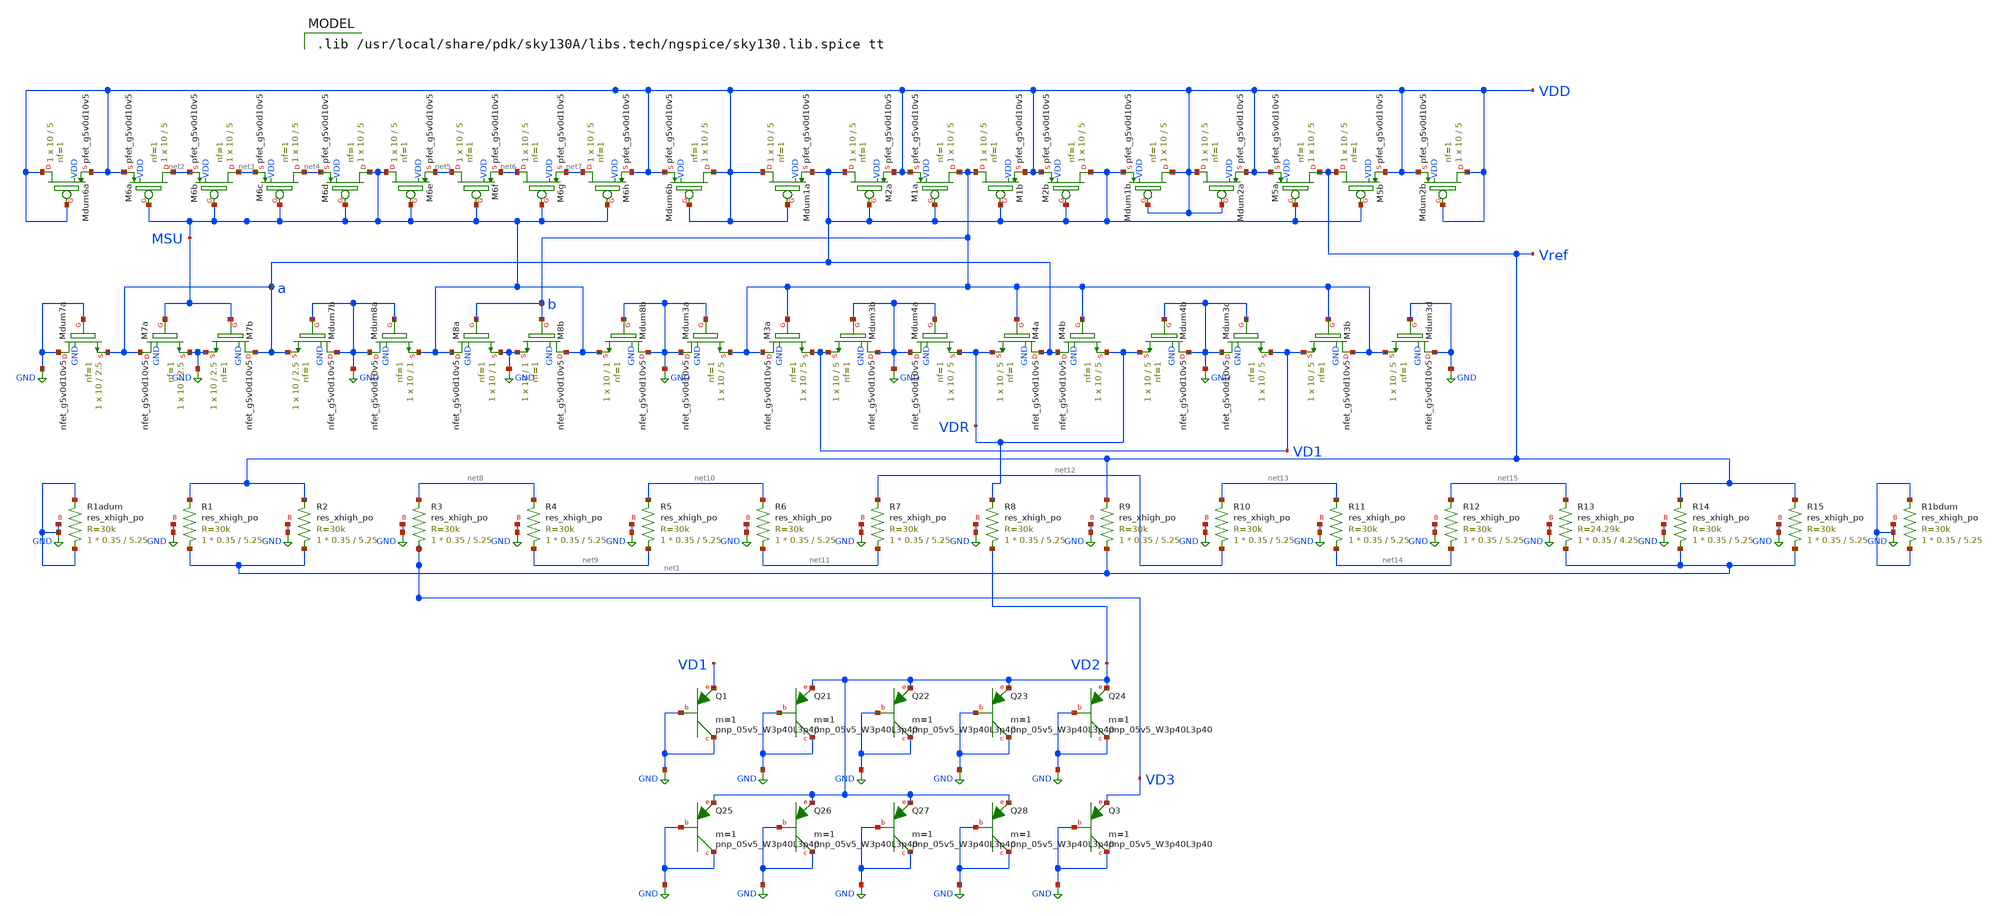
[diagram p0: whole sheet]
** sch_path: 2_BGR_nocas_30k_3p4pnp_floor_Layout.sch
**.subckt 2_BGR_nocas_30k_3p4pnp_floor_Layout
XM2a a a VDD VDD sky130_fd_pr__pfet_g5v0d10v5 L=5 W=10 nf=1 ad='int((nf+1)/2) * W/nf * 0.29' as='int((nf+2)/2) * W/nf * 0.29'
+ pd='2*int((nf+1)/2) * (W/nf + 0.29)' ps='2*int((nf+2)/2) * (W/nf + 0.29)' nrd='0.29 / W' nrs='0.29 / W'
+ sa=0 sb=0 sd=0 mult=1 m=1
XM1a b a VDD VDD sky130_fd_pr__pfet_g5v0d10v5 L=5 W=10 nf=1 ad='int((nf+1)/2) * W/nf * 0.29' as='int((nf+2)/2) * W/nf * 0.29'
+ pd='2*int((nf+1)/2) * (W/nf + 0.29)' ps='2*int((nf+2)/2) * (W/nf + 0.29)' nrd='0.29 / W' nrs='0.29 / W'
+ sa=0 sb=0 sd=0 mult=1 m=1
XM1b b a VDD VDD sky130_fd_pr__pfet_g5v0d10v5 L=5 W=10 nf=1 ad='int((nf+1)/2) * W/nf * 0.29' as='int((nf+2)/2) * W/nf * 0.29'
+ pd='2*int((nf+1)/2) * (W/nf + 0.29)' ps='2*int((nf+2)/2) * (W/nf + 0.29)' nrd='0.29 / W' nrs='0.29 / W'
+ sa=0 sb=0 sd=0 mult=1 m=1
XM2b a a VDD VDD sky130_fd_pr__pfet_g5v0d10v5 L=5 W=10 nf=1 ad='int((nf+1)/2) * W/nf * 0.29' as='int((nf+2)/2) * W/nf * 0.29'
+ pd='2*int((nf+1)/2) * (W/nf + 0.29)' ps='2*int((nf+2)/2) * (W/nf + 0.29)' nrd='0.29 / W' nrs='0.29 / W'
+ sa=0 sb=0 sd=0 mult=1 m=1
XM5a Vref a VDD VDD sky130_fd_pr__pfet_g5v0d10v5 L=5 W=10 nf=1 ad='int((nf+1)/2) * W/nf * 0.29' as='int((nf+2)/2) * W/nf * 0.29'
+ pd='2*int((nf+1)/2) * (W/nf + 0.29)' ps='2*int((nf+2)/2) * (W/nf + 0.29)' nrd='0.29 / W' nrs='0.29 / W'
+ sa=0 sb=0 sd=0 mult=1 m=1
XM5b Vref a VDD VDD sky130_fd_pr__pfet_g5v0d10v5 L=5 W=10 nf=1 ad='int((nf+1)/2) * W/nf * 0.29' as='int((nf+2)/2) * W/nf * 0.29'
+ pd='2*int((nf+1)/2) * (W/nf + 0.29)' ps='2*int((nf+2)/2) * (W/nf + 0.29)' nrd='0.29 / W' nrs='0.29 / W'
+ sa=0 sb=0 sd=0 mult=1 m=1
XQ21 GND GND VD2 sky130_fd_pr__pnp_05v5_W3p40L3p40 m=1
XQ22 GND GND VD2 sky130_fd_pr__pnp_05v5_W3p40L3p40 m=1
XQ23 GND GND VD2 sky130_fd_pr__pnp_05v5_W3p40L3p40 m=1
XQ24 GND GND VD2 sky130_fd_pr__pnp_05v5_W3p40L3p40 m=1
XQ1 GND GND VD1 sky130_fd_pr__pnp_05v5_W3p40L3p40 m=1
XQ26 GND GND VD2 sky130_fd_pr__pnp_05v5_W3p40L3p40 m=1
XQ27 GND GND VD2 sky130_fd_pr__pnp_05v5_W3p40L3p40 m=1
XQ28 GND GND VD2 sky130_fd_pr__pnp_05v5_W3p40L3p40 m=1
XQ3 GND GND VD3 sky130_fd_pr__pnp_05v5_W3p40L3p40 m=1
XQ25 GND GND VD2 sky130_fd_pr__pnp_05v5_W3p40L3p40 m=1
XMdum1a VDD VDD a VDD sky130_fd_pr__pfet_g5v0d10v5 L=5 W=10 nf=1 ad='int((nf+1)/2) * W/nf * 0.29' as='int((nf+2)/2) * W/nf * 0.29'
+ pd='2*int((nf+1)/2) * (W/nf + 0.29)' ps='2*int((nf+2)/2) * (W/nf + 0.29)' nrd='0.29 / W' nrs='0.29 / W'
+ sa=0 sb=0 sd=0 mult=1 m=1
XMdum1b VDD VDD a VDD sky130_fd_pr__pfet_g5v0d10v5 L=5 W=10 nf=1 ad='int((nf+1)/2) * W/nf * 0.29' as='int((nf+2)/2) * W/nf * 0.29'
+ pd='2*int((nf+1)/2) * (W/nf + 0.29)' ps='2*int((nf+2)/2) * (W/nf + 0.29)' nrd='0.29 / W' nrs='0.29 / W'
+ sa=0 sb=0 sd=0 mult=1 m=1
XMdum2a VDD VDD VDD VDD sky130_fd_pr__pfet_g5v0d10v5 L=5 W=10 nf=1 ad='int((nf+1)/2) * W/nf * 0.29' as='int((nf+2)/2) * W/nf * 0.29'
+ pd='2*int((nf+1)/2) * (W/nf + 0.29)' ps='2*int((nf+2)/2) * (W/nf + 0.29)' nrd='0.29 / W' nrs='0.29 / W'
+ sa=0 sb=0 sd=0 mult=1 m=1
XMdum2b VDD VDD VDD VDD sky130_fd_pr__pfet_g5v0d10v5 L=5 W=10 nf=1 ad='int((nf+1)/2) * W/nf * 0.29' as='int((nf+2)/2) * W/nf * 0.29'
+ pd='2*int((nf+1)/2) * (W/nf + 0.29)' ps='2*int((nf+2)/2) * (W/nf + 0.29)' nrd='0.29 / W' nrs='0.29 / W'
+ sa=0 sb=0 sd=0 mult=1 m=1
XM6a net2 MSU VDD VDD sky130_fd_pr__pfet_g5v0d10v5 L=5 W=10 nf=1 ad='int((nf+1)/2) * W/nf * 0.29' as='int((nf+2)/2) * W/nf * 0.29'
+ pd='2*int((nf+1)/2) * (W/nf + 0.29)' ps='2*int((nf+2)/2) * (W/nf + 0.29)' nrd='0.29 / W' nrs='0.29 / W'
+ sa=0 sb=0 sd=0 mult=1 m=1
XM6b net3 MSU net2 VDD sky130_fd_pr__pfet_g5v0d10v5 L=5 W=10 nf=1 ad='int((nf+1)/2) * W/nf * 0.29' as='int((nf+2)/2) * W/nf * 0.29'
+ pd='2*int((nf+1)/2) * (W/nf + 0.29)' ps='2*int((nf+2)/2) * (W/nf + 0.29)' nrd='0.29 / W' nrs='0.29 / W'
+ sa=0 sb=0 sd=0 mult=1 m=1
XM6c net4 MSU net3 VDD sky130_fd_pr__pfet_g5v0d10v5 L=5 W=10 nf=1 ad='int((nf+1)/2) * W/nf * 0.29' as='int((nf+2)/2) * W/nf * 0.29'
+ pd='2*int((nf+1)/2) * (W/nf + 0.29)' ps='2*int((nf+2)/2) * (W/nf + 0.29)' nrd='0.29 / W' nrs='0.29 / W'
+ sa=0 sb=0 sd=0 mult=1 m=1
XM6d MSU MSU net4 VDD sky130_fd_pr__pfet_g5v0d10v5 L=5 W=10 nf=1 ad='int((nf+1)/2) * W/nf * 0.29' as='int((nf+2)/2) * W/nf * 0.29'
+ pd='2*int((nf+1)/2) * (W/nf + 0.29)' ps='2*int((nf+2)/2) * (W/nf + 0.29)' nrd='0.29 / W' nrs='0.29 / W'
+ sa=0 sb=0 sd=0 mult=1 m=1
XM6e MSU MSU net5 VDD sky130_fd_pr__pfet_g5v0d10v5 L=5 W=10 nf=1 ad='int((nf+1)/2) * W/nf * 0.29' as='int((nf+2)/2) * W/nf * 0.29'
+ pd='2*int((nf+1)/2) * (W/nf + 0.29)' ps='2*int((nf+2)/2) * (W/nf + 0.29)' nrd='0.29 / W' nrs='0.29 / W'
+ sa=0 sb=0 sd=0 mult=1 m=1
XM6f net5 MSU net6 VDD sky130_fd_pr__pfet_g5v0d10v5 L=5 W=10 nf=1 ad='int((nf+1)/2) * W/nf * 0.29' as='int((nf+2)/2) * W/nf * 0.29'
+ pd='2*int((nf+1)/2) * (W/nf + 0.29)' ps='2*int((nf+2)/2) * (W/nf + 0.29)' nrd='0.29 / W' nrs='0.29 / W'
+ sa=0 sb=0 sd=0 mult=1 m=1
XM6g net6 MSU net7 VDD sky130_fd_pr__pfet_g5v0d10v5 L=5 W=10 nf=1 ad='int((nf+1)/2) * W/nf * 0.29' as='int((nf+2)/2) * W/nf * 0.29'
+ pd='2*int((nf+1)/2) * (W/nf + 0.29)' ps='2*int((nf+2)/2) * (W/nf + 0.29)' nrd='0.29 / W' nrs='0.29 / W'
+ sa=0 sb=0 sd=0 mult=1 m=1
XM6h net7 MSU VDD VDD sky130_fd_pr__pfet_g5v0d10v5 L=5 W=10 nf=1 ad='int((nf+1)/2) * W/nf * 0.29' as='int((nf+2)/2) * W/nf * 0.29'
+ pd='2*int((nf+1)/2) * (W/nf + 0.29)' ps='2*int((nf+2)/2) * (W/nf + 0.29)' nrd='0.29 / W' nrs='0.29 / W'
+ sa=0 sb=0 sd=0 mult=1 m=1
XMdum6b VDD VDD VDD VDD sky130_fd_pr__pfet_g5v0d10v5 L=5 W=10 nf=1 ad='int((nf+1)/2) * W/nf * 0.29' as='int((nf+2)/2) * W/nf * 0.29'
+ pd='2*int((nf+1)/2) * (W/nf + 0.29)' ps='2*int((nf+2)/2) * (W/nf + 0.29)' nrd='0.29 / W' nrs='0.29 / W'
+ sa=0 sb=0 sd=0 mult=1 m=1
XMdum6a VDD VDD VDD VDD sky130_fd_pr__pfet_g5v0d10v5 L=5 W=10 nf=1 ad='int((nf+1)/2) * W/nf * 0.29' as='int((nf+2)/2) * W/nf * 0.29'
+ pd='2*int((nf+1)/2) * (W/nf + 0.29)' ps='2*int((nf+2)/2) * (W/nf + 0.29)' nrd='0.29 / W' nrs='0.29 / W'
+ sa=0 sb=0 sd=0 mult=1 m=1
XM7a a MSU GND GND sky130_fd_pr__nfet_g5v0d10v5 L=2.5 W=10 nf=1 ad='int((nf+1)/2) * W/nf * 0.29' as='int((nf+2)/2) * W/nf * 0.29'
+ pd='2*int((nf+1)/2) * (W/nf + 0.29)' ps='2*int((nf+2)/2) * (W/nf + 0.29)' nrd='0.29 / W' nrs='0.29 / W'
+ sa=0 sb=0 sd=0 mult=1 m=1
XM7b a MSU GND GND sky130_fd_pr__nfet_g5v0d10v5 L=2.5 W=10 nf=1 ad='int((nf+1)/2) * W/nf * 0.29' as='int((nf+2)/2) * W/nf * 0.29'
+ pd='2*int((nf+1)/2) * (W/nf + 0.29)' ps='2*int((nf+2)/2) * (W/nf + 0.29)' nrd='0.29 / W' nrs='0.29 / W'
+ sa=0 sb=0 sd=0 mult=1 m=1
XMdum7a GND GND a GND sky130_fd_pr__nfet_g5v0d10v5 L=2.5 W=10 nf=1 ad='int((nf+1)/2) * W/nf * 0.29' as='int((nf+2)/2) * W/nf * 0.29'
+ pd='2*int((nf+1)/2) * (W/nf + 0.29)' ps='2*int((nf+2)/2) * (W/nf + 0.29)' nrd='0.29 / W' nrs='0.29 / W'
+ sa=0 sb=0 sd=0 mult=1 m=1
XMdum7b GND GND a GND sky130_fd_pr__nfet_g5v0d10v5 L=2.5 W=10 nf=1 ad='int((nf+1)/2) * W/nf * 0.29' as='int((nf+2)/2) * W/nf * 0.29'
+ pd='2*int((nf+1)/2) * (W/nf + 0.29)' ps='2*int((nf+2)/2) * (W/nf + 0.29)' nrd='0.29 / W' nrs='0.29 / W'
+ sa=0 sb=0 sd=0 mult=1 m=1
XMdum8a GND GND MSU GND sky130_fd_pr__nfet_g5v0d10v5 L=1 W=10 nf=1 ad='int((nf+1)/2) * W/nf * 0.29' as='int((nf+2)/2) * W/nf * 0.29'
+ pd='2*int((nf+1)/2) * (W/nf + 0.29)' ps='2*int((nf+2)/2) * (W/nf + 0.29)' nrd='0.29 / W' nrs='0.29 / W'
+ sa=0 sb=0 sd=0 mult=1 m=1
XM8a MSU b GND GND sky130_fd_pr__nfet_g5v0d10v5 L=1 W=10 nf=1 ad='int((nf+1)/2) * W/nf * 0.29' as='int((nf+2)/2) * W/nf * 0.29'
+ pd='2*int((nf+1)/2) * (W/nf + 0.29)' ps='2*int((nf+2)/2) * (W/nf + 0.29)' nrd='0.29 / W' nrs='0.29 / W'
+ sa=0 sb=0 sd=0 mult=1 m=1
XM8b MSU b GND GND sky130_fd_pr__nfet_g5v0d10v5 L=1 W=10 nf=1 ad='int((nf+1)/2) * W/nf * 0.29' as='int((nf+2)/2) * W/nf * 0.29'
+ pd='2*int((nf+1)/2) * (W/nf + 0.29)' ps='2*int((nf+2)/2) * (W/nf + 0.29)' nrd='0.29 / W' nrs='0.29 / W'
+ sa=0 sb=0 sd=0 mult=1 m=1
XMdum8b GND GND MSU GND sky130_fd_pr__nfet_g5v0d10v5 L=1 W=10 nf=1 ad='int((nf+1)/2) * W/nf * 0.29' as='int((nf+2)/2) * W/nf * 0.29'
+ pd='2*int((nf+1)/2) * (W/nf + 0.29)' ps='2*int((nf+2)/2) * (W/nf + 0.29)' nrd='0.29 / W' nrs='0.29 / W'
+ sa=0 sb=0 sd=0 mult=1 m=1
XMdum3a GND GND b GND sky130_fd_pr__nfet_g5v0d10v5 L=5 W=10 nf=1 ad='int((nf+1)/2) * W/nf * 0.29' as='int((nf+2)/2) * W/nf * 0.29'
+ pd='2*int((nf+1)/2) * (W/nf + 0.29)' ps='2*int((nf+2)/2) * (W/nf + 0.29)' nrd='0.29 / W' nrs='0.29 / W'
+ sa=0 sb=0 sd=0 mult=1 m=1
XM3a b b VD1 GND sky130_fd_pr__nfet_g5v0d10v5 L=5 W=10 nf=1 ad='int((nf+1)/2) * W/nf * 0.29' as='int((nf+2)/2) * W/nf * 0.29'
+ pd='2*int((nf+1)/2) * (W/nf + 0.29)' ps='2*int((nf+2)/2) * (W/nf + 0.29)' nrd='0.29 / W' nrs='0.29 / W'
+ sa=0 sb=0 sd=0 mult=1 m=1
XMdum3b GND GND VD1 GND sky130_fd_pr__nfet_g5v0d10v5 L=5 W=10 nf=1 ad='int((nf+1)/2) * W/nf * 0.29' as='int((nf+2)/2) * W/nf * 0.29'
+ pd='2*int((nf+1)/2) * (W/nf + 0.29)' ps='2*int((nf+2)/2) * (W/nf + 0.29)' nrd='0.29 / W' nrs='0.29 / W'
+ sa=0 sb=0 sd=0 mult=1 m=1
XMdum4a GND GND VDR GND sky130_fd_pr__nfet_g5v0d10v5 L=5 W=10 nf=1 ad='int((nf+1)/2) * W/nf * 0.29' as='int((nf+2)/2) * W/nf * 0.29'
+ pd='2*int((nf+1)/2) * (W/nf + 0.29)' ps='2*int((nf+2)/2) * (W/nf + 0.29)' nrd='0.29 / W' nrs='0.29 / W'
+ sa=0 sb=0 sd=0 mult=1 m=1
XM4a a b VDR GND sky130_fd_pr__nfet_g5v0d10v5 L=5 W=10 nf=1 ad='int((nf+1)/2) * W/nf * 0.29' as='int((nf+2)/2) * W/nf * 0.29'
+ pd='2*int((nf+1)/2) * (W/nf + 0.29)' ps='2*int((nf+2)/2) * (W/nf + 0.29)' nrd='0.29 / W' nrs='0.29 / W'
+ sa=0 sb=0 sd=0 mult=1 m=1
XM4b a b VDR GND sky130_fd_pr__nfet_g5v0d10v5 L=5 W=10 nf=1 ad='int((nf+1)/2) * W/nf * 0.29' as='int((nf+2)/2) * W/nf * 0.29'
+ pd='2*int((nf+1)/2) * (W/nf + 0.29)' ps='2*int((nf+2)/2) * (W/nf + 0.29)' nrd='0.29 / W' nrs='0.29 / W'
+ sa=0 sb=0 sd=0 mult=1 m=1
XMdum4b GND GND VDR GND sky130_fd_pr__nfet_g5v0d10v5 L=5 W=10 nf=1 ad='int((nf+1)/2) * W/nf * 0.29' as='int((nf+2)/2) * W/nf * 0.29'
+ pd='2*int((nf+1)/2) * (W/nf + 0.29)' ps='2*int((nf+2)/2) * (W/nf + 0.29)' nrd='0.29 / W' nrs='0.29 / W'
+ sa=0 sb=0 sd=0 mult=1 m=1
XMdum3c GND GND VD1 GND sky130_fd_pr__nfet_g5v0d10v5 L=5 W=10 nf=1 ad='int((nf+1)/2) * W/nf * 0.29' as='int((nf+2)/2) * W/nf * 0.29'
+ pd='2*int((nf+1)/2) * (W/nf + 0.29)' ps='2*int((nf+2)/2) * (W/nf + 0.29)' nrd='0.29 / W' nrs='0.29 / W'
+ sa=0 sb=0 sd=0 mult=1 m=1
XM3b b b VD1 GND sky130_fd_pr__nfet_g5v0d10v5 L=5 W=10 nf=1 ad='int((nf+1)/2) * W/nf * 0.29' as='int((nf+2)/2) * W/nf * 0.29'
+ pd='2*int((nf+1)/2) * (W/nf + 0.29)' ps='2*int((nf+2)/2) * (W/nf + 0.29)' nrd='0.29 / W' nrs='0.29 / W'
+ sa=0 sb=0 sd=0 mult=1 m=1
XMdum3d GND GND b GND sky130_fd_pr__nfet_g5v0d10v5 L=5 W=10 nf=1 ad='int((nf+1)/2) * W/nf * 0.29' as='int((nf+2)/2) * W/nf * 0.29'
+ pd='2*int((nf+1)/2) * (W/nf + 0.29)' ps='2*int((nf+2)/2) * (W/nf + 0.29)' nrd='0.29 / W' nrs='0.29 / W'
+ sa=0 sb=0 sd=0 mult=1 m=1
XR1 net1 Vref GND sky130_fd_pr__res_xhigh_po W=0.35 L=5.25 mult=1 m=1
XR2 net1 Vref GND sky130_fd_pr__res_xhigh_po W=0.35 L=5.25 mult=1 m=1
XR3 VD3 net8 GND sky130_fd_pr__res_xhigh_po W=0.35 L=5.25 mult=1 m=1
XR4 net9 net8 GND sky130_fd_pr__res_xhigh_po W=0.35 L=5.25 mult=1 m=1
XR5 net9 net10 GND sky130_fd_pr__res_xhigh_po W=0.35 L=5.25 mult=1 m=1
XR6 net11 net10 GND sky130_fd_pr__res_xhigh_po W=0.35 L=5.25 mult=1 m=1
XR7 net11 net12 GND sky130_fd_pr__res_xhigh_po W=0.35 L=5.25 mult=1 m=1
XR8 VD2 VDR GND sky130_fd_pr__res_xhigh_po W=0.35 L=5.25 mult=1 m=1
XR9 net1 Vref GND sky130_fd_pr__res_xhigh_po W=0.35 L=5.25 mult=1 m=1
XR10 net12 net13 GND sky130_fd_pr__res_xhigh_po W=0.35 L=5.25 mult=1 m=1
XR11 net14 net13 GND sky130_fd_pr__res_xhigh_po W=0.35 L=5.25 mult=1 m=1
XR12 net14 net15 GND sky130_fd_pr__res_xhigh_po W=0.35 L=5.25 mult=1 m=1
XR13 net1 net15 GND sky130_fd_pr__res_xhigh_po W=0.35 L=4.25 mult=1 m=1
XR14 net1 Vref GND sky130_fd_pr__res_xhigh_po W=0.35 L=5.25 mult=1 m=1
XR15 net1 Vref GND sky130_fd_pr__res_xhigh_po W=0.35 L=5.25 mult=1 m=1
XR1bdum GND GND GND sky130_fd_pr__res_xhigh_po W=0.35 L=5.25 mult=1 m=1
XR1adum GND GND GND sky130_fd_pr__res_xhigh_po W=0.35 L=5.25 mult=1 m=1
**** begin user architecture code

.save all
Vdd Vdd 0 DC 0 AC 0
*** Plot color settings***
.control
set color0=white  color1=black color2=blue color3=red
set color4=magenta  color5=cyan  xbrushwidth=3
.endc
*** Temp variation ***
.control
alter Vdd DC=3.3
dc temp -40 125 0.1
plot V1#branch V2#branch V3#branch
plot VD3
plot V(Vref,VD3)
plot Vref
.endc
************************
*** Supply variation ***
.control
dc Vdd 2 5.5 1m
plot Vref Vdd
.endc
************************
*** PSRR analysis ***
.control
alter Vdd DC=3.3
alter Vdd AC=1
ac dec 10 1 10G
plot db(Vref)
.endc
*************************
*** Transient analysis ***
.control
alter @Vdd[pwl]=[ 0 0 100u 0 200u 3.3 500u 3.3 ]
tran 100u 500u
plot Vdd Vref
.endc
*************************
.end


.lib /usr/local/share/pdk/sky130A/libs.tech/ngspice/sky130.lib.spice tt

**** end user architecture code
**.ends
.GLOBAL GND
.end
